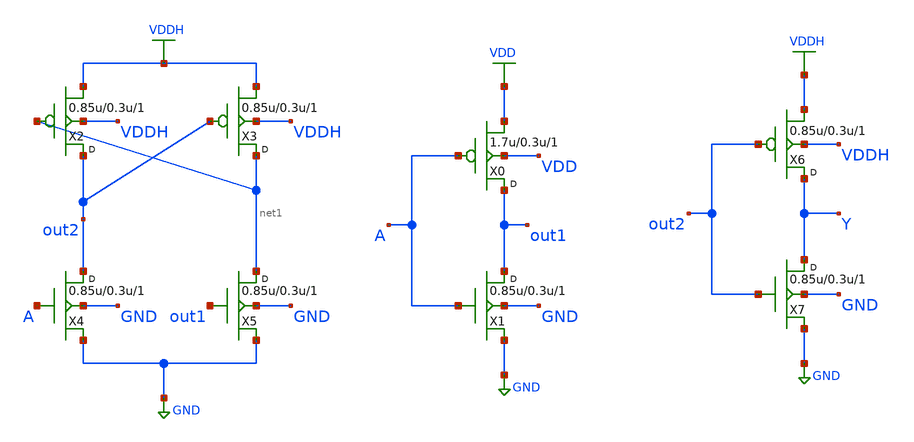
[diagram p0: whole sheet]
** sch_path: lib/12T/lshifup/gf180mcu_osu_sc_lshifup.sch
**.subckt gf180mcu_osu_sc_lshifup
X0 out1 A VDD VDD pmos_3p3 w=1.7u l=0.3u m=1
X1 out1 A GND GND nmos_3p3 w=0.85u l=0.3u m=1
X2 out2 net1 VDDH VDDH pmos_3p3 w=0.85u l=0.3u m=1
X3 net1 out2 VDDH VDDH pmos_3p3 w=0.85u l=0.3u m=1
X4 out2 A GND GND nmos_3p3 w=0.85u l=0.3u m=1
X5 net1 out1 GND GND nmos_3p3 w=0.85u l=0.3u m=1
X6 Y out2 VDDH VDDH pmos_3p3 w=0.85u l=0.3u m=1
X7 Y out2 GND GND nmos_3p3 w=0.85u l=0.3u m=1
**.ends
.GLOBAL VDD
.GLOBAL GND
.GLOBAL VDDH
.end
